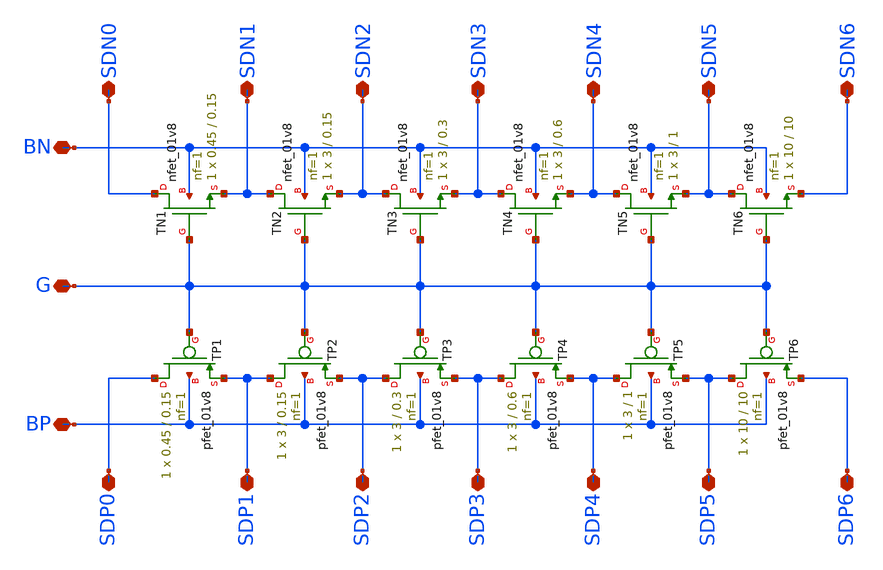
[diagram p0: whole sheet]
** sch_path: char/char.sch
**.subckt char G BN BP SDP0 SDP1 SDP2 SDP3 SDP4 SDP5 SDP6 SDN0 SDN1 SDN2 SDN3 SDN4 SDN5 SDN6
*.iopin G
*.iopin BN
*.iopin BP
*.iopin SDP0
*.iopin SDP1
*.iopin SDP2
*.iopin SDP3
*.iopin SDP4
*.iopin SDP5
*.iopin SDP6
*.iopin SDN0
*.iopin SDN1
*.iopin SDN2
*.iopin SDN3
*.iopin SDN4
*.iopin SDN5
*.iopin SDN6
XTN1 SDN0 G SDN1 BN sky130_fd_pr__nfet_01v8 L=0.15 W=0.45 nf=1 ad='int((nf+1)/2) * W/nf * 0.29' as='int((nf+2)/2) * W/nf * 0.29'
+ pd='2*int((nf+1)/2) * (W/nf + 0.29)' ps='2*int((nf+2)/2) * (W/nf + 0.29)' nrd='0.29 / W' nrs='0.29 / W'
+ sa=0 sb=0 sd=0 mult=1 m=1
XTP1 SDP0 G SDP1 BP sky130_fd_pr__pfet_01v8 L=0.15 W=0.45 nf=1 ad='int((nf+1)/2) * W/nf * 0.29' as='int((nf+2)/2) * W/nf * 0.29'
+ pd='2*int((nf+1)/2) * (W/nf + 0.29)' ps='2*int((nf+2)/2) * (W/nf + 0.29)' nrd='0.29 / W' nrs='0.29 / W'
+ sa=0 sb=0 sd=0 mult=1 m=1
XTN2 SDN1 G SDN2 BN sky130_fd_pr__nfet_01v8 L=0.15 W=3 nf=1 ad='int((nf+1)/2) * W/nf * 0.29' as='int((nf+2)/2) * W/nf * 0.29'
+ pd='2*int((nf+1)/2) * (W/nf + 0.29)' ps='2*int((nf+2)/2) * (W/nf + 0.29)' nrd='0.29 / W' nrs='0.29 / W'
+ sa=0 sb=0 sd=0 mult=1 m=1
XTN3 SDN2 G SDN3 BN sky130_fd_pr__nfet_01v8 L=0.3 W=3 nf=1 ad='int((nf+1)/2) * W/nf * 0.29' as='int((nf+2)/2) * W/nf * 0.29'
+ pd='2*int((nf+1)/2) * (W/nf + 0.29)' ps='2*int((nf+2)/2) * (W/nf + 0.29)' nrd='0.29 / W' nrs='0.29 / W'
+ sa=0 sb=0 sd=0 mult=1 m=1
XTN4 SDN3 G SDN4 BN sky130_fd_pr__nfet_01v8 L=0.6 W=3 nf=1 ad='int((nf+1)/2) * W/nf * 0.29' as='int((nf+2)/2) * W/nf * 0.29'
+ pd='2*int((nf+1)/2) * (W/nf + 0.29)' ps='2*int((nf+2)/2) * (W/nf + 0.29)' nrd='0.29 / W' nrs='0.29 / W'
+ sa=0 sb=0 sd=0 mult=1 m=1
XTN5 SDN4 G SDN5 BN sky130_fd_pr__nfet_01v8 L=1 W=3 nf=1 ad='int((nf+1)/2) * W/nf * 0.29' as='int((nf+2)/2) * W/nf * 0.29'
+ pd='2*int((nf+1)/2) * (W/nf + 0.29)' ps='2*int((nf+2)/2) * (W/nf + 0.29)' nrd='0.29 / W' nrs='0.29 / W'
+ sa=0 sb=0 sd=0 mult=1 m=1
XTN6 SDN5 G SDN6 BN sky130_fd_pr__nfet_01v8 L=10 W=10 nf=1 ad='int((nf+1)/2) * W/nf * 0.29' as='int((nf+2)/2) * W/nf * 0.29'
+ pd='2*int((nf+1)/2) * (W/nf + 0.29)' ps='2*int((nf+2)/2) * (W/nf + 0.29)' nrd='0.29 / W' nrs='0.29 / W'
+ sa=0 sb=0 sd=0 mult=1 m=1
XTP2 SDP1 G SDP2 BP sky130_fd_pr__pfet_01v8 L=0.15 W=3 nf=1 ad='int((nf+1)/2) * W/nf * 0.29' as='int((nf+2)/2) * W/nf * 0.29'
+ pd='2*int((nf+1)/2) * (W/nf + 0.29)' ps='2*int((nf+2)/2) * (W/nf + 0.29)' nrd='0.29 / W' nrs='0.29 / W'
+ sa=0 sb=0 sd=0 mult=1 m=1
XTP3 SDP2 G SDP3 BP sky130_fd_pr__pfet_01v8 L=0.3 W=3 nf=1 ad='int((nf+1)/2) * W/nf * 0.29' as='int((nf+2)/2) * W/nf * 0.29'
+ pd='2*int((nf+1)/2) * (W/nf + 0.29)' ps='2*int((nf+2)/2) * (W/nf + 0.29)' nrd='0.29 / W' nrs='0.29 / W'
+ sa=0 sb=0 sd=0 mult=1 m=1
XTP4 SDP3 G SDP4 BP sky130_fd_pr__pfet_01v8 L=0.6 W=3 nf=1 ad='int((nf+1)/2) * W/nf * 0.29' as='int((nf+2)/2) * W/nf * 0.29'
+ pd='2*int((nf+1)/2) * (W/nf + 0.29)' ps='2*int((nf+2)/2) * (W/nf + 0.29)' nrd='0.29 / W' nrs='0.29 / W'
+ sa=0 sb=0 sd=0 mult=1 m=1
XTP5 SDP4 G SDP5 BP sky130_fd_pr__pfet_01v8 L=1 W=3 nf=1 ad='int((nf+1)/2) * W/nf * 0.29' as='int((nf+2)/2) * W/nf * 0.29'
+ pd='2*int((nf+1)/2) * (W/nf + 0.29)' ps='2*int((nf+2)/2) * (W/nf + 0.29)' nrd='0.29 / W' nrs='0.29 / W'
+ sa=0 sb=0 sd=0 mult=1 m=1
XTP6 SDP5 G SDP6 BP sky130_fd_pr__pfet_01v8 L=10 W=10 nf=1 ad='int((nf+1)/2) * W/nf * 0.29' as='int((nf+2)/2) * W/nf * 0.29'
+ pd='2*int((nf+1)/2) * (W/nf + 0.29)' ps='2*int((nf+2)/2) * (W/nf + 0.29)' nrd='0.29 / W' nrs='0.29 / W'
+ sa=0 sb=0 sd=0 mult=1 m=1
**.ends
.end
